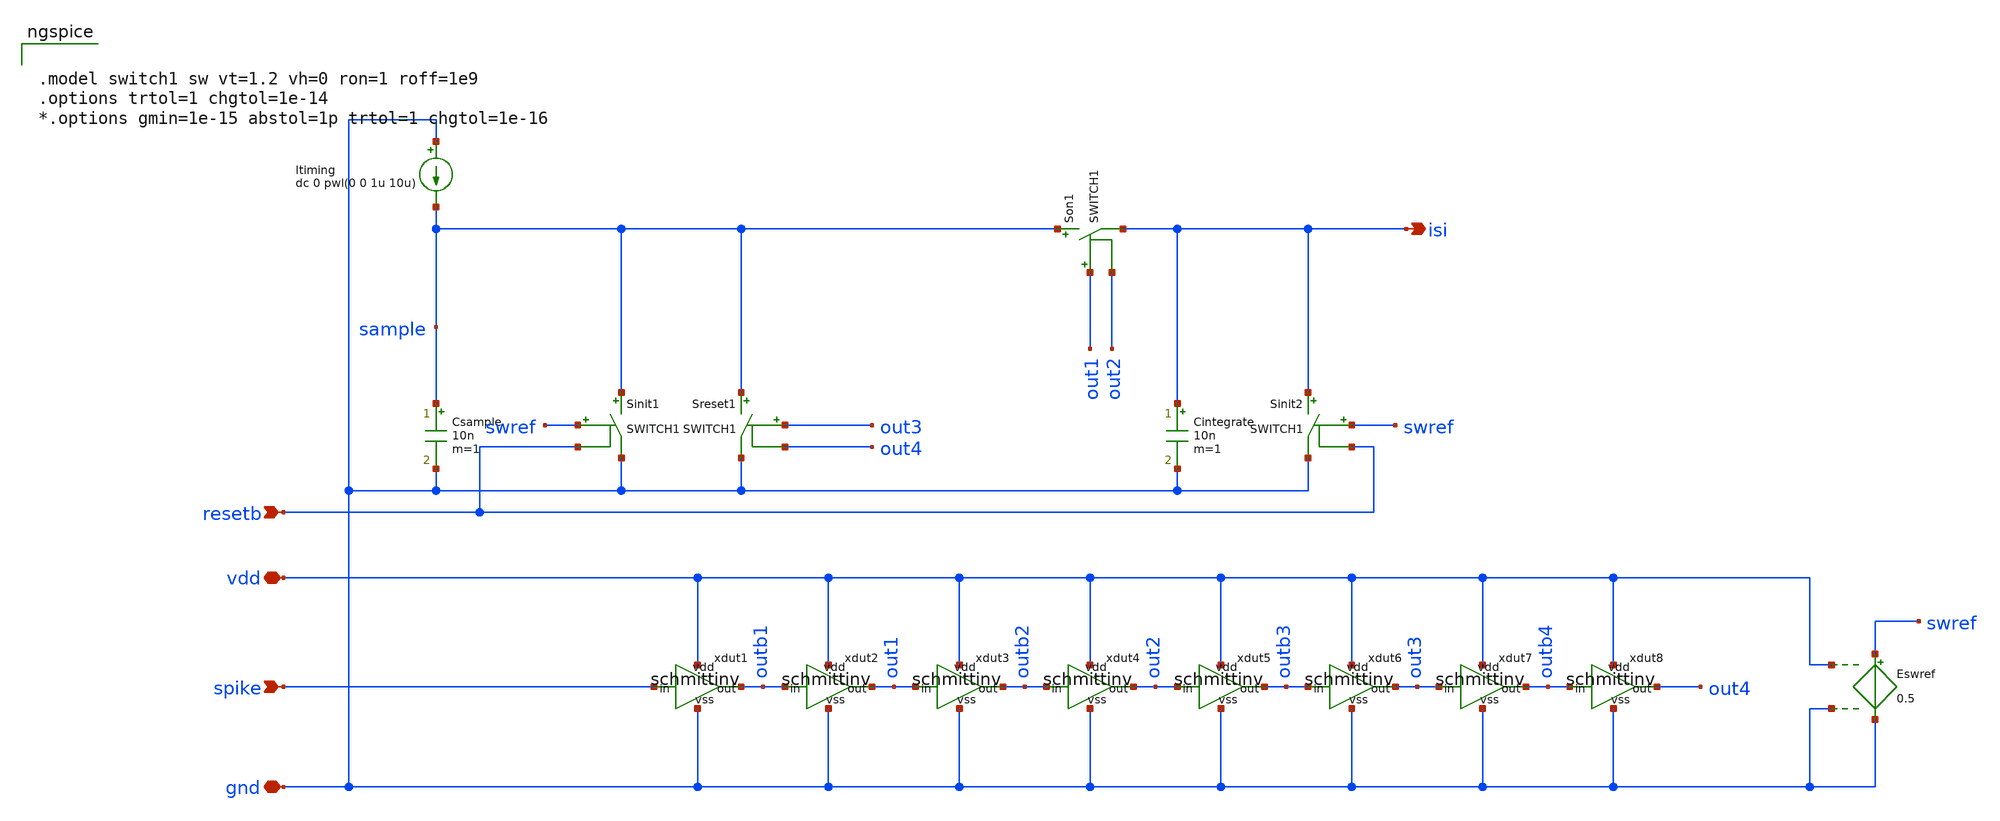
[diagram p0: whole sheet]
** sch_path: playground/InterServicesIntelligence.sch
* Copyright 2020 Stefan Frederik Schippers
* Licensed under the Apache License, Version 2.0 (the "License");
* you may not use this file except in compliance with the License.
* You may obtain a copy of the License at
* https://www.apache.org/licenses/LICENSE-2.0
* Unless required by applicable law or agreed to in writing, software
* distributed under the License is distributed on an "AS IS" BASIS,
* WITHOUT WARRANTIES OR CONDITIONS OF ANY KIND, either express or implied.
* See the License for the specific language governing permissions and
* limitations under the License.
**.subckt InterServicesIntelligence vdd gnd spike isi resetb
*.iopin vdd
*.iopin gnd
*.ipin spike
*.opin isi
*.ipin resetb
xdut1 vdd spike outb1 gnd schmittinv
xdut2 vdd outb1 out1 gnd schmittinv
xdut3 vdd out1 outb2 gnd schmittinv
xdut4 vdd outb2 out2 gnd schmittinv
Csample sample gnd 10n m=1
Itiming gnd sample dc 0 pwl(0 0 1u 10u)
Cintegrate isi gnd 10n m=1
Sreset1 sample gnd out3 out4 SWITCH1
Eswref swref gnd vdd gnd 0.5
Son1 sample isi out1 out2 SWITCH1
Sinit1 sample gnd swref resetb SWITCH1
Sinit2 isi gnd swref resetb SWITCH1
xdut5 vdd out2 outb3 gnd schmittinv
xdut6 vdd outb3 out3 gnd schmittinv
xdut7 vdd out3 outb4 gnd schmittinv
xdut8 vdd outb4 out4 gnd schmittinv
**** begin user architecture code


.model switch1 sw vt=1.2 vh=0 ron=1 roff=1e9
.options trtol=1 chgtol=1e-14
*.options gmin=1e-15 abstol=1p trtol=1 chgtol=1e-16


**** end user architecture code
**.ends

* expanding   symbol:  schmittinv.sym # of pins=4
** sym_path: playground/schmittinv.sym
** sch_path: playground/schmittinv.sch
.subckt schmittinv vdd in out vss
*.iopin vdd
*.iopin vss
*.ipin in
*.opin out
XM1 dn in vss vss sky130_fd_pr__nfet_01v8 L=32 W=0.5 nf=1 ad='int((1 + 1)/2) * 0.5 / 1 * 0.29' as='int((1 + 2)/2) * 0.5 / 1 * 0.29'
+ pd='2*int((1 + 1)/2) * (0.5 / 1 + 0.29)' ps='2*int((1 + 2)/2) * (0.5 / 1 + 0.29)' nrd='0.29 / 0.5 ' nrs='0.29 / 0.5 '
+ sa=0 sb=0 sd=0 mult=1 m=1
XM5 dp in vdd vdd sky130_fd_pr__pfet_01v8 L=16 W=0.5 nf=1 ad='int((nf+1)/2) * W/nf * 0.29' as='int((nf+2)/2) * W/nf * 0.29'
+ pd='2*int((nf+1)/2) * (W/nf + 0.29)' ps='2*int((nf+2)/2) * (W/nf + 0.29)' nrd='0.29 / W' nrs='0.29 / W'
+ sa=0 sb=0 sd=0 mult=1 m=1
XM3 vdd out dn vss sky130_fd_pr__nfet_01v8 L=96 W=0.5 nf=1 ad='int((1 + 1)/2) * 0.5 / 1 * 0.29' as='int((1 + 2)/2) * 0.5 / 1 * 0.29'
+ pd='2*int((1 + 1)/2) * (0.5 / 1 + 0.29)' ps='2*int((1 + 2)/2) * (0.5 / 1 + 0.29)' nrd='0.29 / 0.5 ' nrs='0.29 / 0.5 '
+ sa=0 sb=0 sd=0 mult=1 m=1
XM6 vss out dp vdd sky130_fd_pr__pfet_01v8 L=48 W=0.5 nf=1 ad='int((nf+1)/2) * W/nf * 0.29' as='int((nf+2)/2) * W/nf * 0.29'
+ pd='2*int((nf+1)/2) * (W/nf + 0.29)' ps='2*int((nf+2)/2) * (W/nf + 0.29)' nrd='0.29 / W' nrs='0.29 / W'
+ sa=0 sb=0 sd=0 mult=1 m=1
XM4 out in dp vdd sky130_fd_pr__pfet_01v8 L=16 W=0.5 nf=1 ad='int((nf+1)/2) * W/nf * 0.29' as='int((nf+2)/2) * W/nf * 0.29'
+ pd='2*int((nf+1)/2) * (W/nf + 0.29)' ps='2*int((nf+2)/2) * (W/nf + 0.29)' nrd='0.29 / W' nrs='0.29 / W'
+ sa=0 sb=0 sd=0 mult=1 m=1
XM2 out in dn vss sky130_fd_pr__nfet_01v8 L=32 W=0.5 nf=1 ad='int((1 + 1)/2) * 0.5 / 1 * 0.29' as='int((1 + 2)/2) * 0.5 / 1 * 0.29'
+ pd='2*int((1 + 1)/2) * (0.5 / 1 + 0.29)' ps='2*int((1 + 2)/2) * (0.5 / 1 + 0.29)' nrd='0.29 / 0.5 ' nrs='0.29 / 0.5 '
+ sa=0 sb=0 sd=0 mult=1 m=1
.ends

.end
